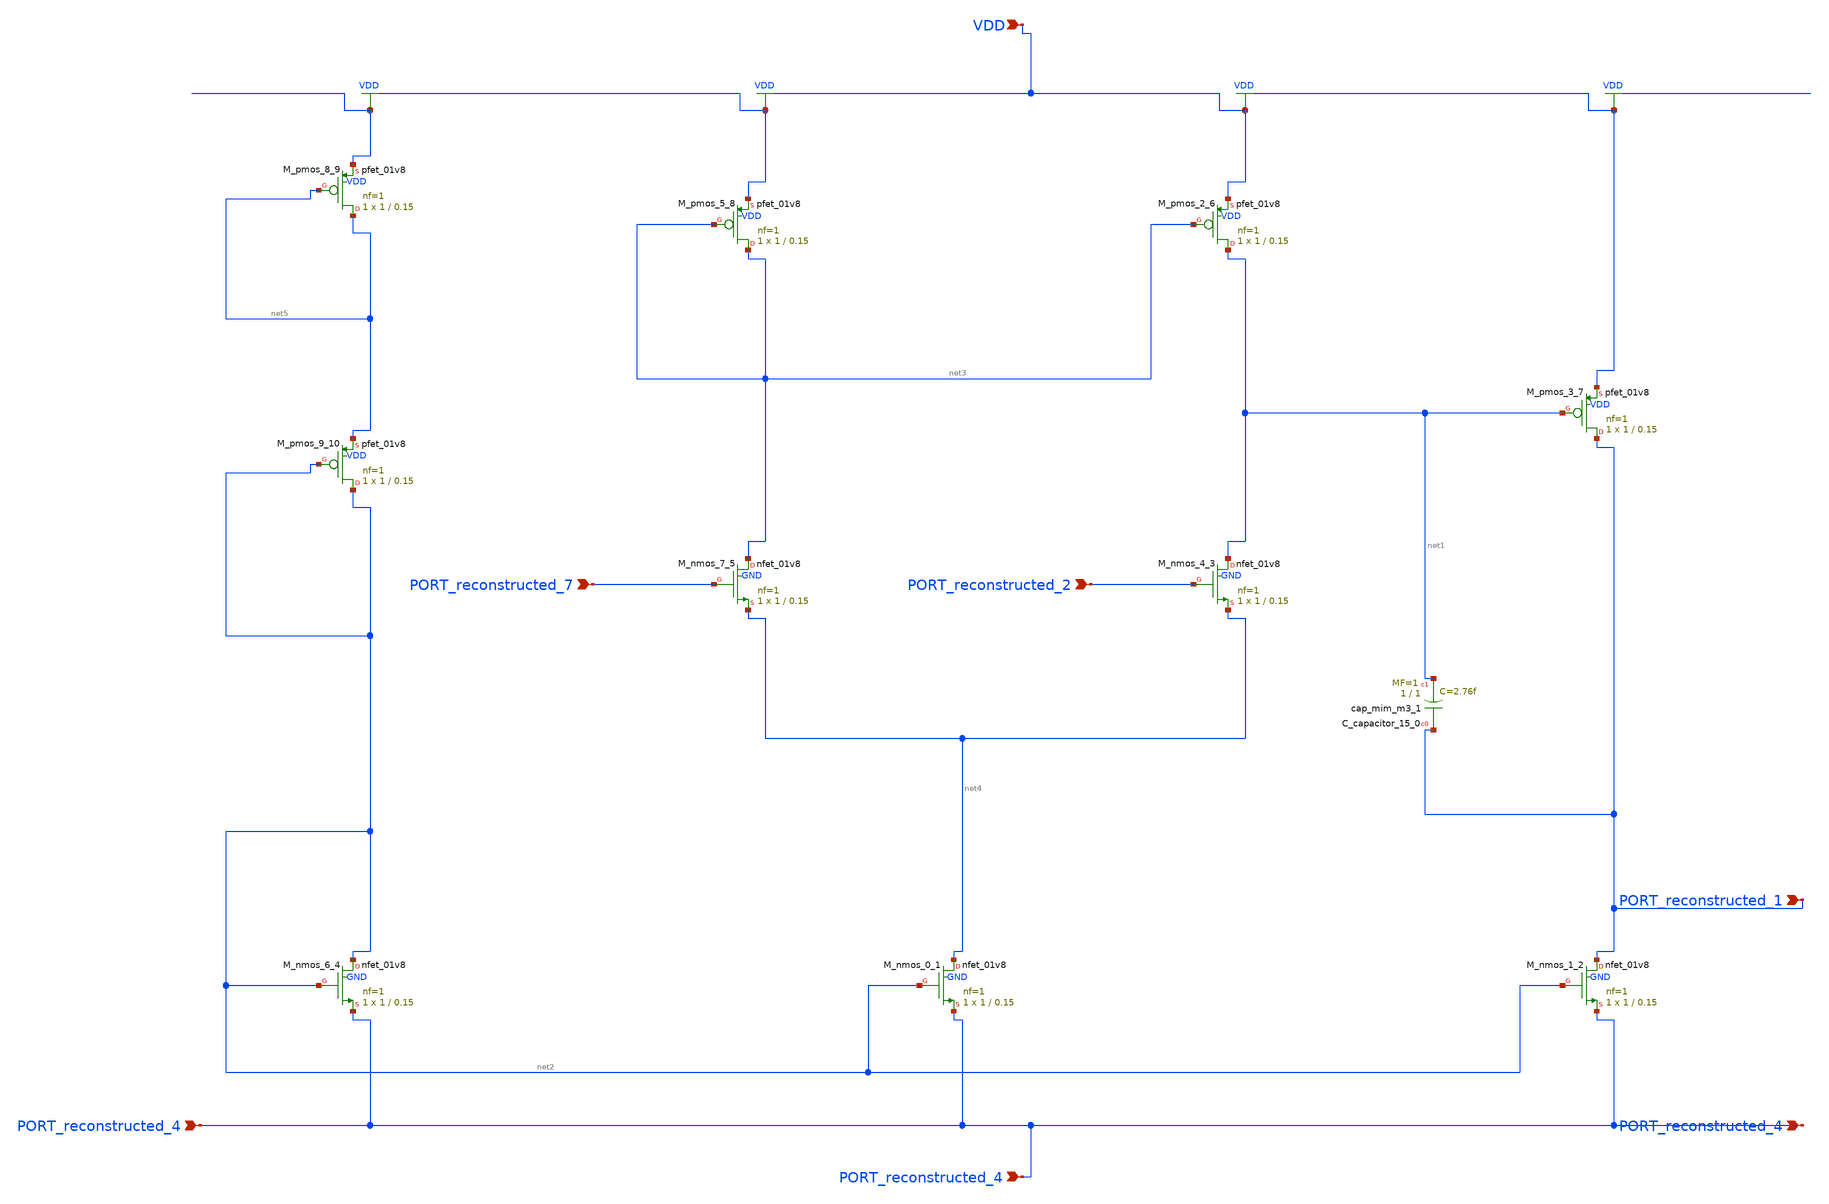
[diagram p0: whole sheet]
** sch_path: schematics/10_1007_s40747-016-0027-3_03_001_canvas.sch
**.subckt 10_1007_s40747-016-0027-3_03_001_canvas VDD PORT_reconstructed_7 PORT_reconstructed_4
*+ PORT_reconstructed_2 PORT_reconstructed_1 PORT_reconstructed_4 PORT_reconstructed_4
*.ipin VDD
*.ipin PORT_reconstructed_7
*.ipin PORT_reconstructed_4
*.ipin PORT_reconstructed_2
*.ipin PORT_reconstructed_1
*.ipin PORT_reconstructed_4
*.ipin PORT_reconstructed_4
XC_capacitor_15_0 PORT_reconstructed_1 net1 sky130_fd_pr__cap_mim_m3_1 W=1 L=1 MF=1 m=1
XM_nmos_0_1 net4 net2 PORT_reconstructed_4 GND sky130_fd_pr__nfet_01v8 L=0.15 W=1 nf=1 ad='int((1 + 1)/2) * 1 / 1 * 0.29'
+ as='int((1 + 2)/2) * 1 / 1 * 0.29' pd='2*int((1 + 1)/2) * (1 / 1 + 0.29)' ps='2*int((1 + 2)/2) * (1 / 1 + 0.29)'
+ nrd='0.29 / 1 ' nrs='0.29 / 1 ' sa=0 sb=0 sd=0 mult=1 m=1
XM_nmos_1_2 PORT_reconstructed_1 net2 PORT_reconstructed_4 GND sky130_fd_pr__nfet_01v8 L=0.15 W=1 nf=1
+ ad='int((1 + 1)/2) * 1 / 1 * 0.29' as='int((1 + 2)/2) * 1 / 1 * 0.29' pd='2*int((1 + 1)/2) * (1 / 1 + 0.29)'
+ ps='2*int((1 + 2)/2) * (1 / 1 + 0.29)' nrd='0.29 / 1 ' nrs='0.29 / 1 ' sa=0 sb=0 sd=0 mult=1 m=1
XM_nmos_4_3 net1 PORT_reconstructed_2 net4 GND sky130_fd_pr__nfet_01v8 L=0.15 W=1 nf=1 ad='int((1 + 1)/2) * 1 / 1 * 0.29'
+ as='int((1 + 2)/2) * 1 / 1 * 0.29' pd='2*int((1 + 1)/2) * (1 / 1 + 0.29)' ps='2*int((1 + 2)/2) * (1 / 1 + 0.29)'
+ nrd='0.29 / 1 ' nrs='0.29 / 1 ' sa=0 sb=0 sd=0 mult=1 m=1
XM_nmos_6_4 net2 net2 PORT_reconstructed_4 GND sky130_fd_pr__nfet_01v8 L=0.15 W=1 nf=1 ad='int((1 + 1)/2) * 1 / 1 * 0.29'
+ as='int((1 + 2)/2) * 1 / 1 * 0.29' pd='2*int((1 + 1)/2) * (1 / 1 + 0.29)' ps='2*int((1 + 2)/2) * (1 / 1 + 0.29)'
+ nrd='0.29 / 1 ' nrs='0.29 / 1 ' sa=0 sb=0 sd=0 mult=1 m=1
XM_nmos_7_5 net3 PORT_reconstructed_7 net4 GND sky130_fd_pr__nfet_01v8 L=0.15 W=1 nf=1 ad='int((1 + 1)/2) * 1 / 1 * 0.29'
+ as='int((1 + 2)/2) * 1 / 1 * 0.29' pd='2*int((1 + 1)/2) * (1 / 1 + 0.29)' ps='2*int((1 + 2)/2) * (1 / 1 + 0.29)'
+ nrd='0.29 / 1 ' nrs='0.29 / 1 ' sa=0 sb=0 sd=0 mult=1 m=1
XM_pmos_2_6 net1 net3 VDD VDD sky130_fd_pr__pfet_01v8 L=0.15 W=1 nf=1 ad='int((1 + 1)/2) * 1 / 1 * 0.29'
+ as='int((1 + 2)/2) * 1 / 1 * 0.29' pd='2*int((1 + 1)/2) * (1 / 1 + 0.29)' ps='2*int((1 + 2)/2) * (1 / 1 + 0.29)'
+ nrd='0.29 / 1 ' nrs='0.29 / 1 ' sa=0 sb=0 sd=0 mult=1 m=1
XM_pmos_3_7 PORT_reconstructed_1 net1 VDD VDD sky130_fd_pr__pfet_01v8 L=0.15 W=1 nf=1 ad='int((1 + 1)/2) * 1 / 1 * 0.29'
+ as='int((1 + 2)/2) * 1 / 1 * 0.29' pd='2*int((1 + 1)/2) * (1 / 1 + 0.29)' ps='2*int((1 + 2)/2) * (1 / 1 + 0.29)'
+ nrd='0.29 / 1 ' nrs='0.29 / 1 ' sa=0 sb=0 sd=0 mult=1 m=1
XM_pmos_5_8 net3 net3 VDD VDD sky130_fd_pr__pfet_01v8 L=0.15 W=1 nf=1 ad='int((1 + 1)/2) * 1 / 1 * 0.29'
+ as='int((1 + 2)/2) * 1 / 1 * 0.29' pd='2*int((1 + 1)/2) * (1 / 1 + 0.29)' ps='2*int((1 + 2)/2) * (1 / 1 + 0.29)'
+ nrd='0.29 / 1 ' nrs='0.29 / 1 ' sa=0 sb=0 sd=0 mult=1 m=1
XM_pmos_8_9 net5 net5 VDD VDD sky130_fd_pr__pfet_01v8 L=0.15 W=1 nf=1 ad='int((1 + 1)/2) * 1 / 1 * 0.29'
+ as='int((1 + 2)/2) * 1 / 1 * 0.29' pd='2*int((1 + 1)/2) * (1 / 1 + 0.29)' ps='2*int((1 + 2)/2) * (1 / 1 + 0.29)'
+ nrd='0.29 / 1 ' nrs='0.29 / 1 ' sa=0 sb=0 sd=0 mult=1 m=1
XM_pmos_9_10 net2 net2 net5 VDD sky130_fd_pr__pfet_01v8 L=0.15 W=1 nf=1 ad='int((1 + 1)/2) * 1 / 1 * 0.29'
+ as='int((1 + 2)/2) * 1 / 1 * 0.29' pd='2*int((1 + 1)/2) * (1 / 1 + 0.29)' ps='2*int((1 + 2)/2) * (1 / 1 + 0.29)'
+ nrd='0.29 / 1 ' nrs='0.29 / 1 ' sa=0 sb=0 sd=0 mult=1 m=1
**.ends
.GLOBAL VDD
.end
